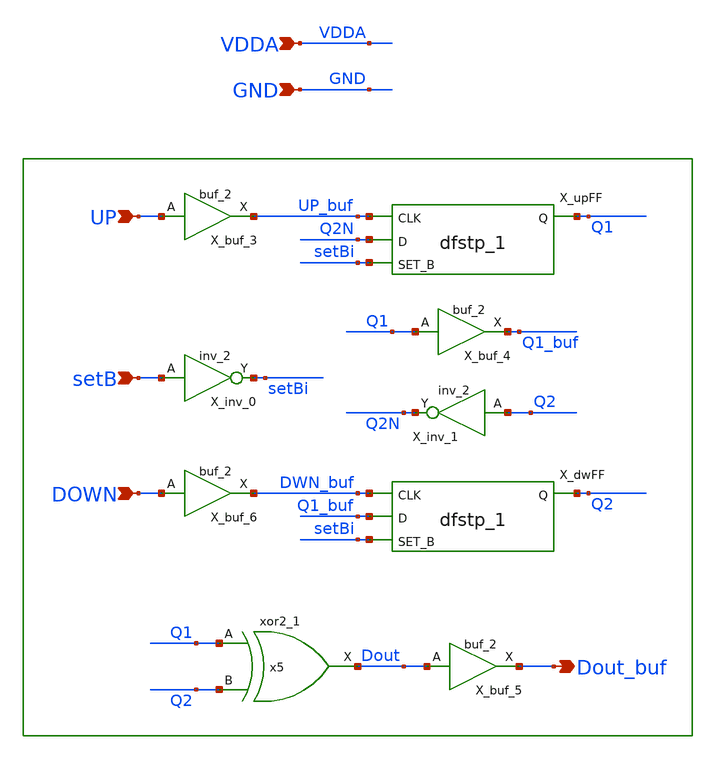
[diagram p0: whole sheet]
** sch_path: xschem/lib/DLib_UpDownCounter.sch
**.subckt DLib_UpDownCounter DOWN Dout_buf GND setB UP VDDA
*.ipin DOWN
*.opin Dout_buf
*.ipin GND
*.ipin setB
*.ipin UP
*.ipin VDDA
X_inv_0 setB GND GND VDDA VDDA setBi sky130_fd_sc_hd__inv_2
X_upFF UP_buf Q2N setBi GND GND VDDA VDDA Q1 sky130_fd_sc_hd__dfstp_1
X_dwFF DWN_buf Q1_buf setBi GND GND VDDA VDDA Q2 sky130_fd_sc_hd__dfstp_1
x5 Q1 Q2 GND GND VDDA VDDA Dout sky130_fd_sc_hd__xor2_1
X_buf_3 UP GND GND VDDA VDDA UP_buf sky130_fd_sc_hd__buf_2
X_buf_4 Q1 GND GND VDDA VDDA Q1_buf sky130_fd_sc_hd__buf_2
X_buf_5 Dout GND GND VDDA VDDA Dout_buf sky130_fd_sc_hd__buf_2
X_buf_6 DOWN GND GND VDDA VDDA DWN_buf sky130_fd_sc_hd__buf_2
X_inv_1 Q2 GND GND VDDA VDDA Q2N sky130_fd_sc_hd__inv_2
**.ends
.end
